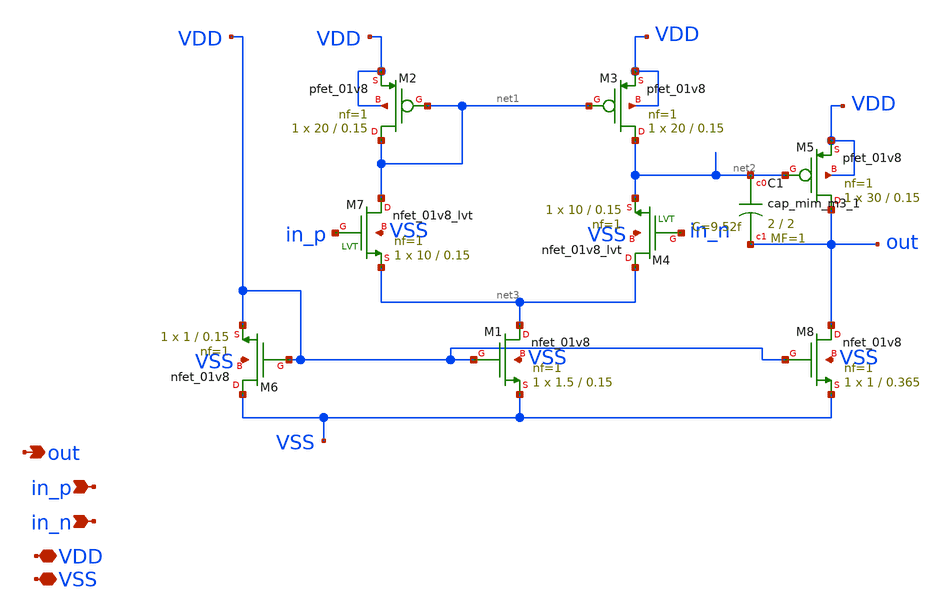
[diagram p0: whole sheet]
** sch_path: xschem/src/ota/ota.sch
**.subckt ota VDD in_p out VSS in_n
*.iopin VDD
*.ipin in_p
*.opin out
*.iopin VSS
*.ipin in_n
XM1 net3 VDD VSS VSS sky130_fd_pr__nfet_01v8 L=0.15 W=1.5 nf=1 ad='int((nf+1)/2) * W/nf * 0.29' as='int((nf+2)/2) * W/nf * 0.29'
+ pd='2*int((nf+1)/2) * (W/nf + 0.29)' ps='2*int((nf+2)/2) * (W/nf + 0.29)' nrd='0.29 / W' nrs='0.29 / W'
+ sa=0 sb=0 sd=0 mult=1 m=1
XM2 net1 net1 VDD VDD sky130_fd_pr__pfet_01v8 L=0.15 W=20 nf=1 ad='int((nf+1)/2) * W/nf * 0.29' as='int((nf+2)/2) * W/nf * 0.29'
+ pd='2*int((nf+1)/2) * (W/nf + 0.29)' ps='2*int((nf+2)/2) * (W/nf + 0.29)' nrd='0.29 / W' nrs='0.29 / W'
+ sa=0 sb=0 sd=0 mult=1 m=1
XM3 net2 net1 VDD VDD sky130_fd_pr__pfet_01v8 L=0.15 W=20 nf=1 ad='int((nf+1)/2) * W/nf * 0.29' as='int((nf+2)/2) * W/nf * 0.29'
+ pd='2*int((nf+1)/2) * (W/nf + 0.29)' ps='2*int((nf+2)/2) * (W/nf + 0.29)' nrd='0.29 / W' nrs='0.29 / W'
+ sa=0 sb=0 sd=0 mult=1 m=1
XM6 VSS VDD VDD VSS sky130_fd_pr__nfet_01v8 L=0.15 W=1 nf=1 ad='int((nf+1)/2) * W/nf * 0.29' as='int((nf+2)/2) * W/nf * 0.29'
+ pd='2*int((nf+1)/2) * (W/nf + 0.29)' ps='2*int((nf+2)/2) * (W/nf + 0.29)' nrd='0.29 / W' nrs='0.29 / W'
+ sa=0 sb=0 sd=0 mult=1 m=1
XM7 net1 in_p net3 VSS sky130_fd_pr__nfet_01v8_lvt L=0.15 W=10 nf=1 ad='int((nf+1)/2) * W/nf * 0.29'
+ as='int((nf+2)/2) * W/nf * 0.29' pd='2*int((nf+1)/2) * (W/nf + 0.29)' ps='2*int((nf+2)/2) * (W/nf + 0.29)'
+ nrd='0.29 / W' nrs='0.29 / W' sa=0 sb=0 sd=0 mult=1 m=1
XM4 net3 in_n net2 VSS sky130_fd_pr__nfet_01v8_lvt L=0.15 W=10 nf=1 ad='int((nf+1)/2) * W/nf * 0.29'
+ as='int((nf+2)/2) * W/nf * 0.29' pd='2*int((nf+1)/2) * (W/nf + 0.29)' ps='2*int((nf+2)/2) * (W/nf + 0.29)'
+ nrd='0.29 / W' nrs='0.29 / W' sa=0 sb=0 sd=0 mult=1 m=1
XM8 out VDD VSS VSS sky130_fd_pr__nfet_01v8 L=0.365 W=1 nf=1 ad='int((nf+1)/2) * W/nf * 0.29' as='int((nf+2)/2) * W/nf * 0.29'
+ pd='2*int((nf+1)/2) * (W/nf + 0.29)' ps='2*int((nf+2)/2) * (W/nf + 0.29)' nrd='0.29 / W' nrs='0.29 / W'
+ sa=0 sb=0 sd=0 mult=1 m=1
XM5 out net2 VDD VDD sky130_fd_pr__pfet_01v8 L=0.15 W=30 nf=1 ad='int((nf+1)/2) * W/nf * 0.29' as='int((nf+2)/2) * W/nf * 0.29'
+ pd='2*int((nf+1)/2) * (W/nf + 0.29)' ps='2*int((nf+2)/2) * (W/nf + 0.29)' nrd='0.29 / W' nrs='0.29 / W'
+ sa=0 sb=0 sd=0 mult=1 m=1
XC1 net2 out sky130_fd_pr__cap_mim_m3_1 W=2 L=2 MF=1 m=1
**.ends
.end
